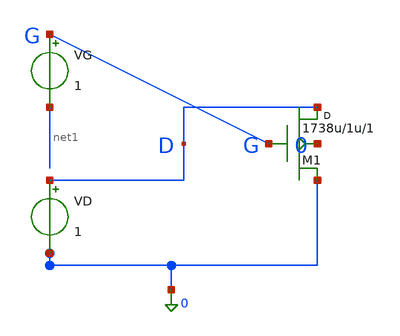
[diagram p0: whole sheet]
** sch_path: nmos_dc_sweeps.sch
**.subckt nmos_dc_sweeps
M1 D G 0 0 ALD1101 w=1738u l=1u m=1
VG G net1 1
VD D 0 1
**** begin user architecture code

.MODEL ALD1101 NMOS LEVEL = 2 UO = 12.72 VTO = 0.6766 NFS = 1.154E12 TOX = 1E-08 NSUB = 3.892E17
+ UCRIT = 4.582E05 UEXP = 0.07025 VMAX = 6363 RS = 9.491 RD = 5.659 XJ = 4.787E-09 LD = 0 DELTA = 1E-12
+ NEFF = 0.8345 NSS = -3.801 CGSO = 1.15E-9 CGDO = 1.15E-9 CGBO = 0 CBD = 0 CBS = 0 CJ = 0 MJ = 0.5  CJSW
+ = 0 MJSW = 0.6057 IS = 1.0E-14 PB = 0.8 FC = 0.5 NEFF=5



.dc VD 0 3 0.01




.dc VG 0 3 0.01


**** end user architecture code
**.ends
.end
